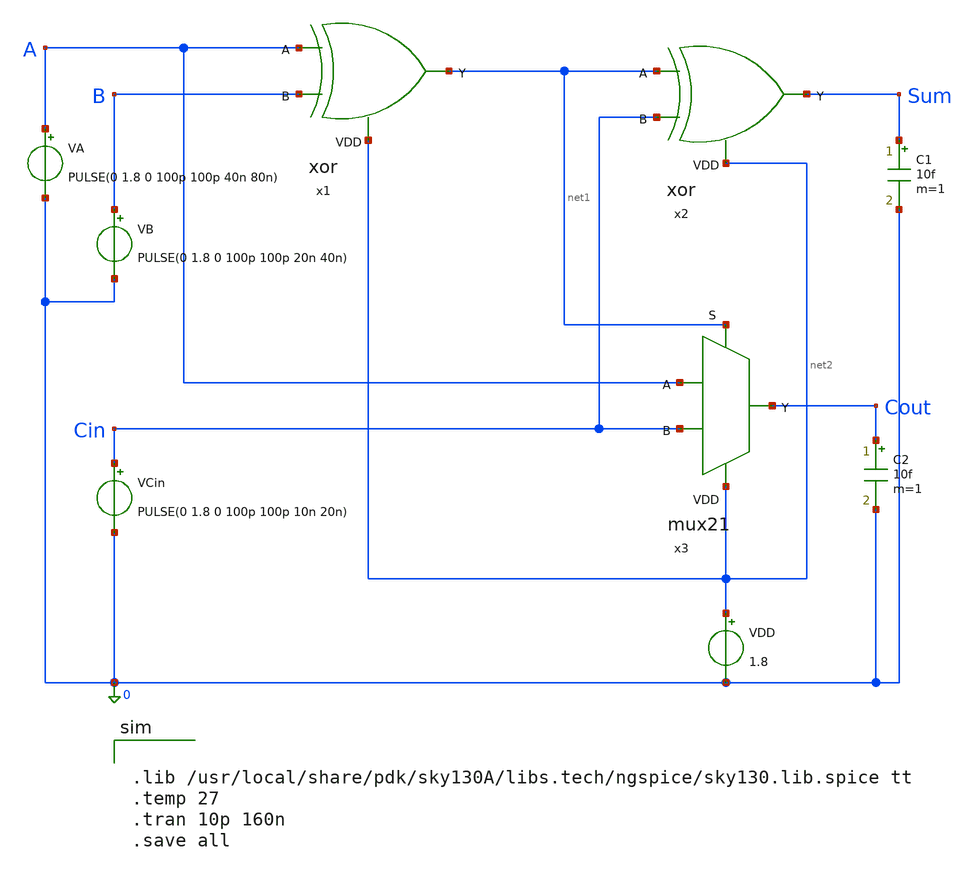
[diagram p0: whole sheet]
** sch_path: schematic/fulladder.sch
**.subckt fulladder
x1 net2 A net1 B xor
x2 net2 net1 Sum Cin xor
x3 A net1 Cout Cin net2 mux21
VB B 0 PULSE(0 1.8 0 100p 100p 20n 40n)
VA A 0 PULSE(0 1.8 0 100p 100p 40n 80n)
VDD net2 0 1.8
VCin Cin 0 PULSE(0 1.8 0 100p 100p 10n 20n)
C1 Sum 0 10f m=1
C2 Cout 0 10f m=1
**** begin user architecture code


.lib /usr/local/share/pdk/sky130A/libs.tech/ngspice/sky130.lib.spice tt
.temp 27
.tran 10p 160n
.save all


**** end user architecture code
**.ends
.end
